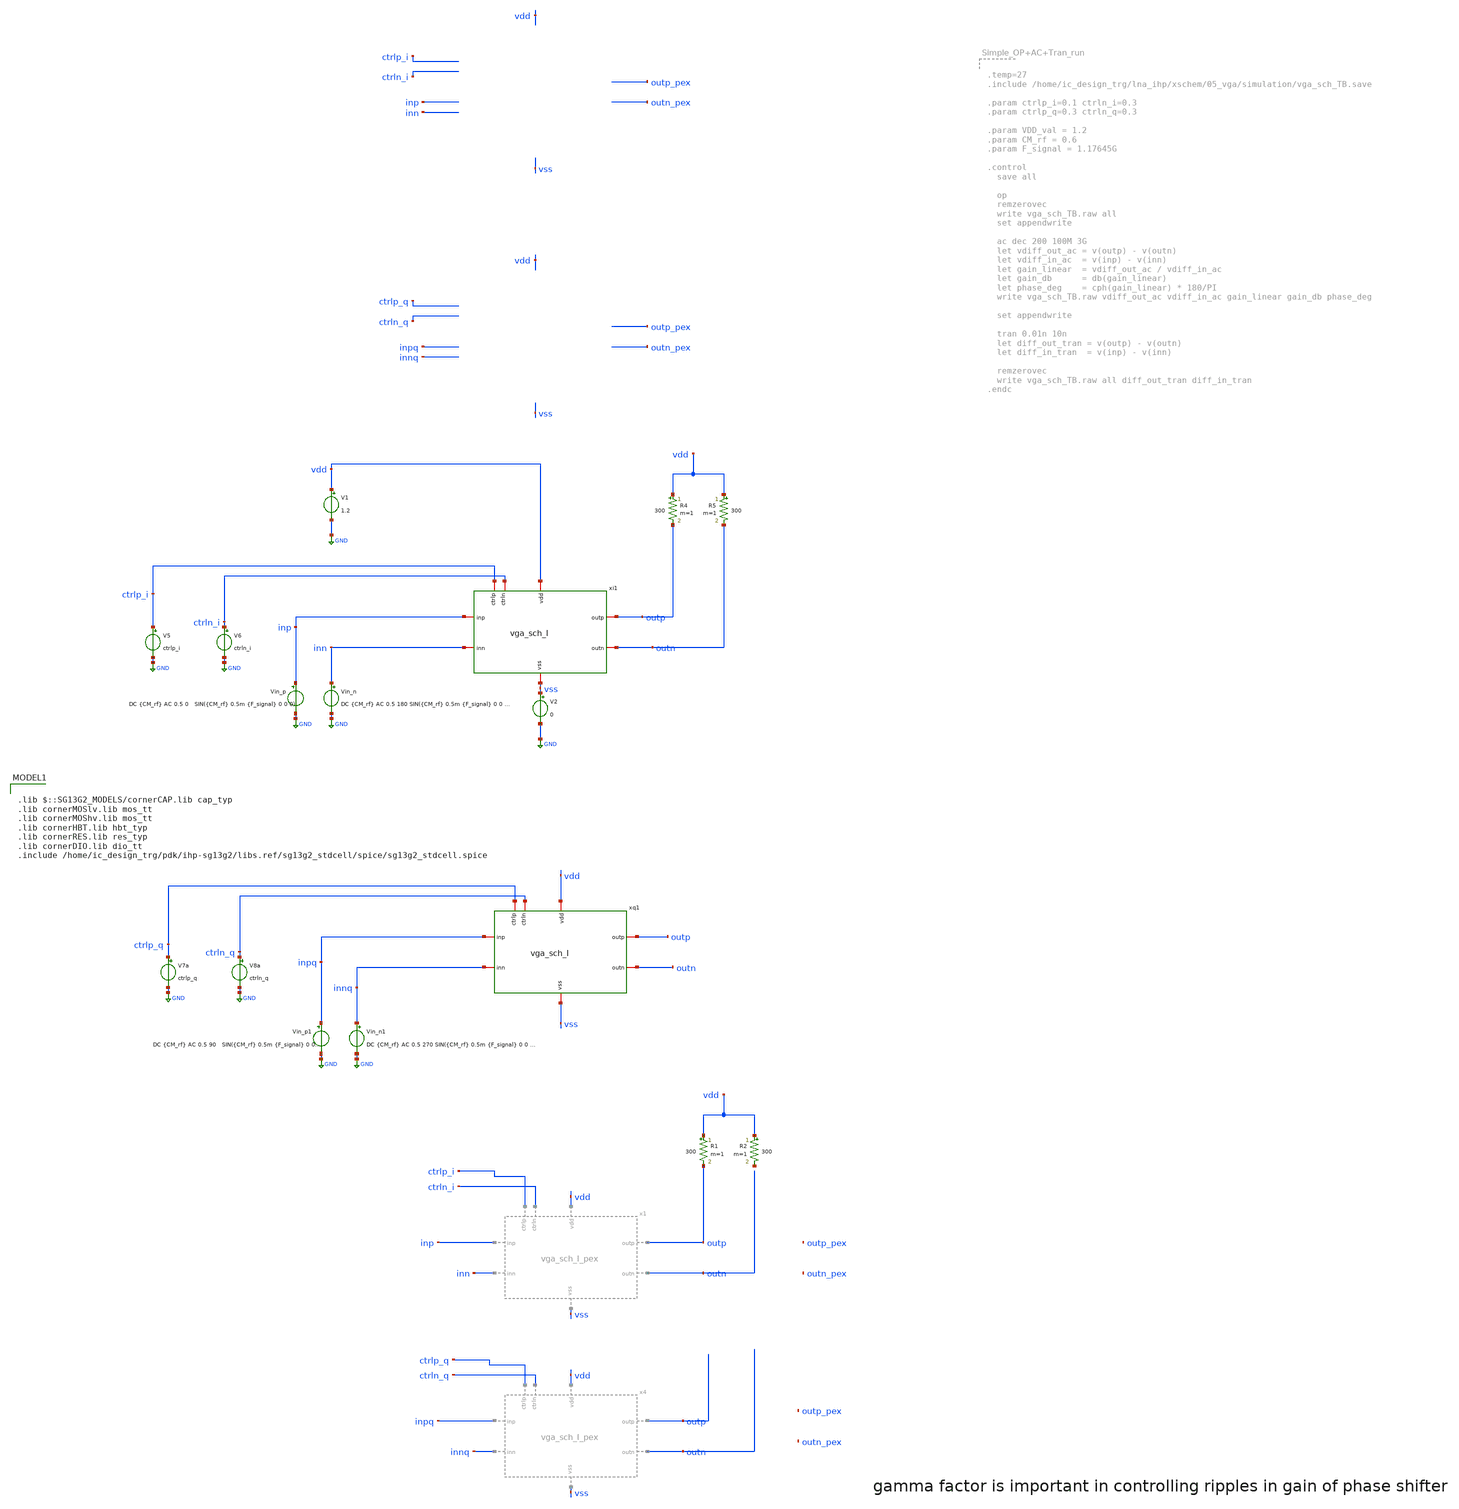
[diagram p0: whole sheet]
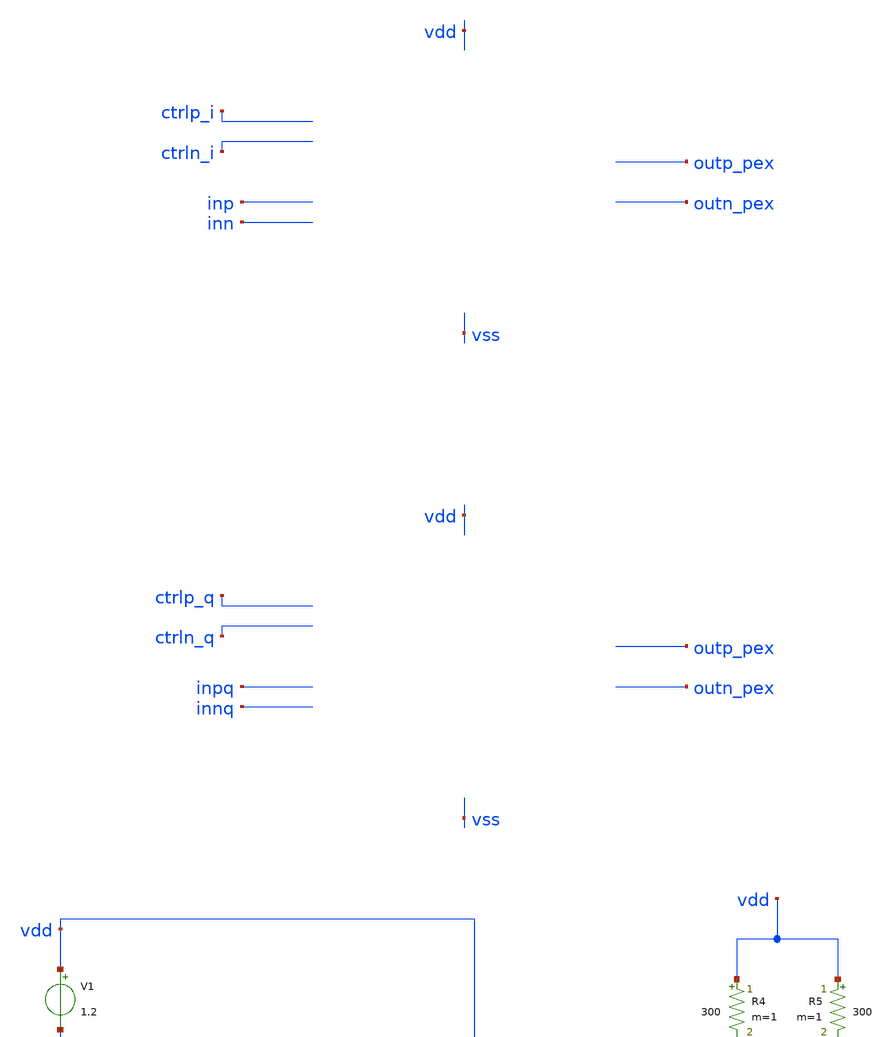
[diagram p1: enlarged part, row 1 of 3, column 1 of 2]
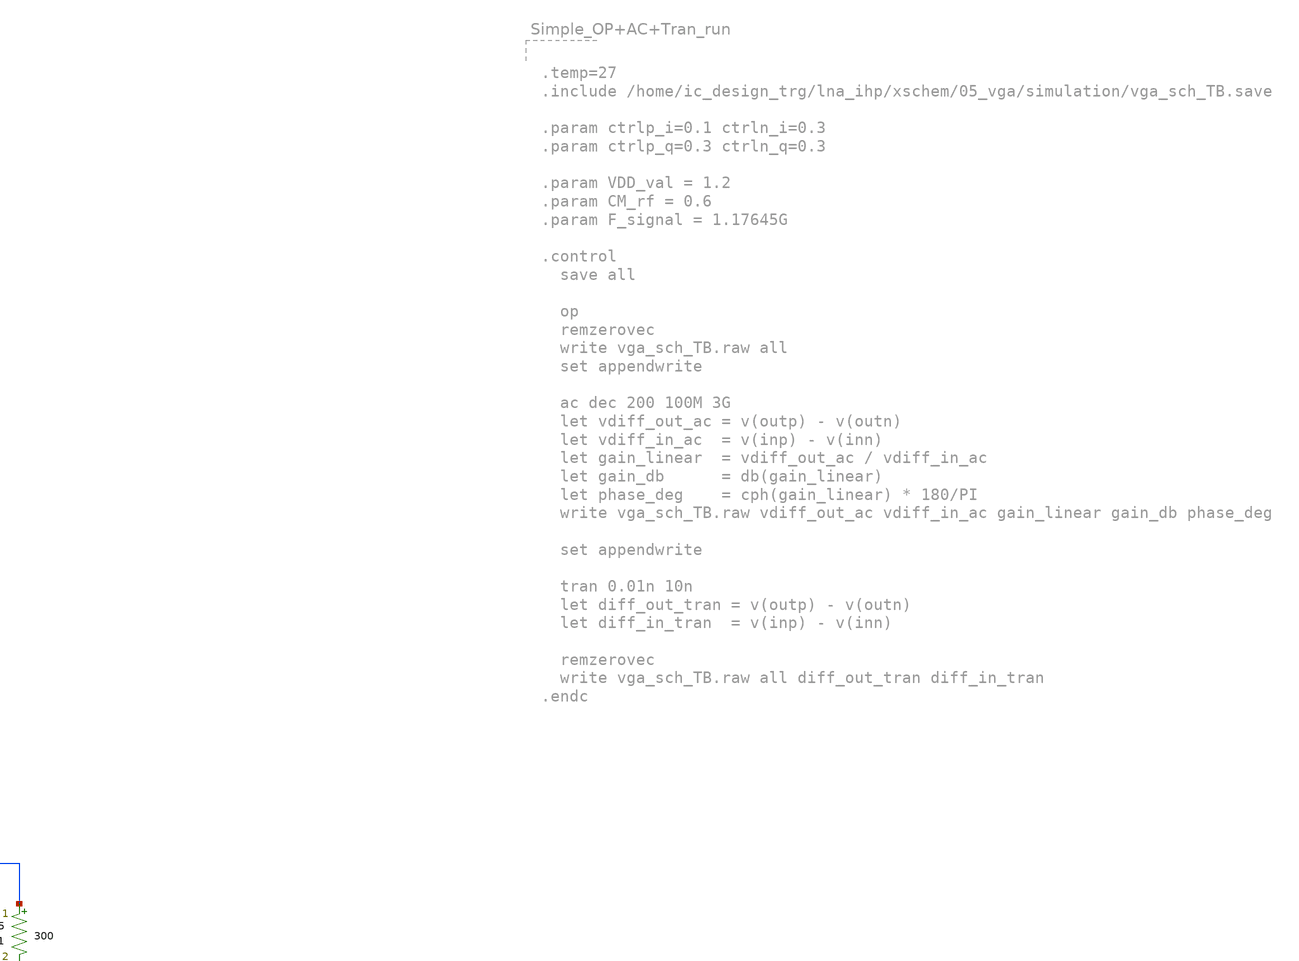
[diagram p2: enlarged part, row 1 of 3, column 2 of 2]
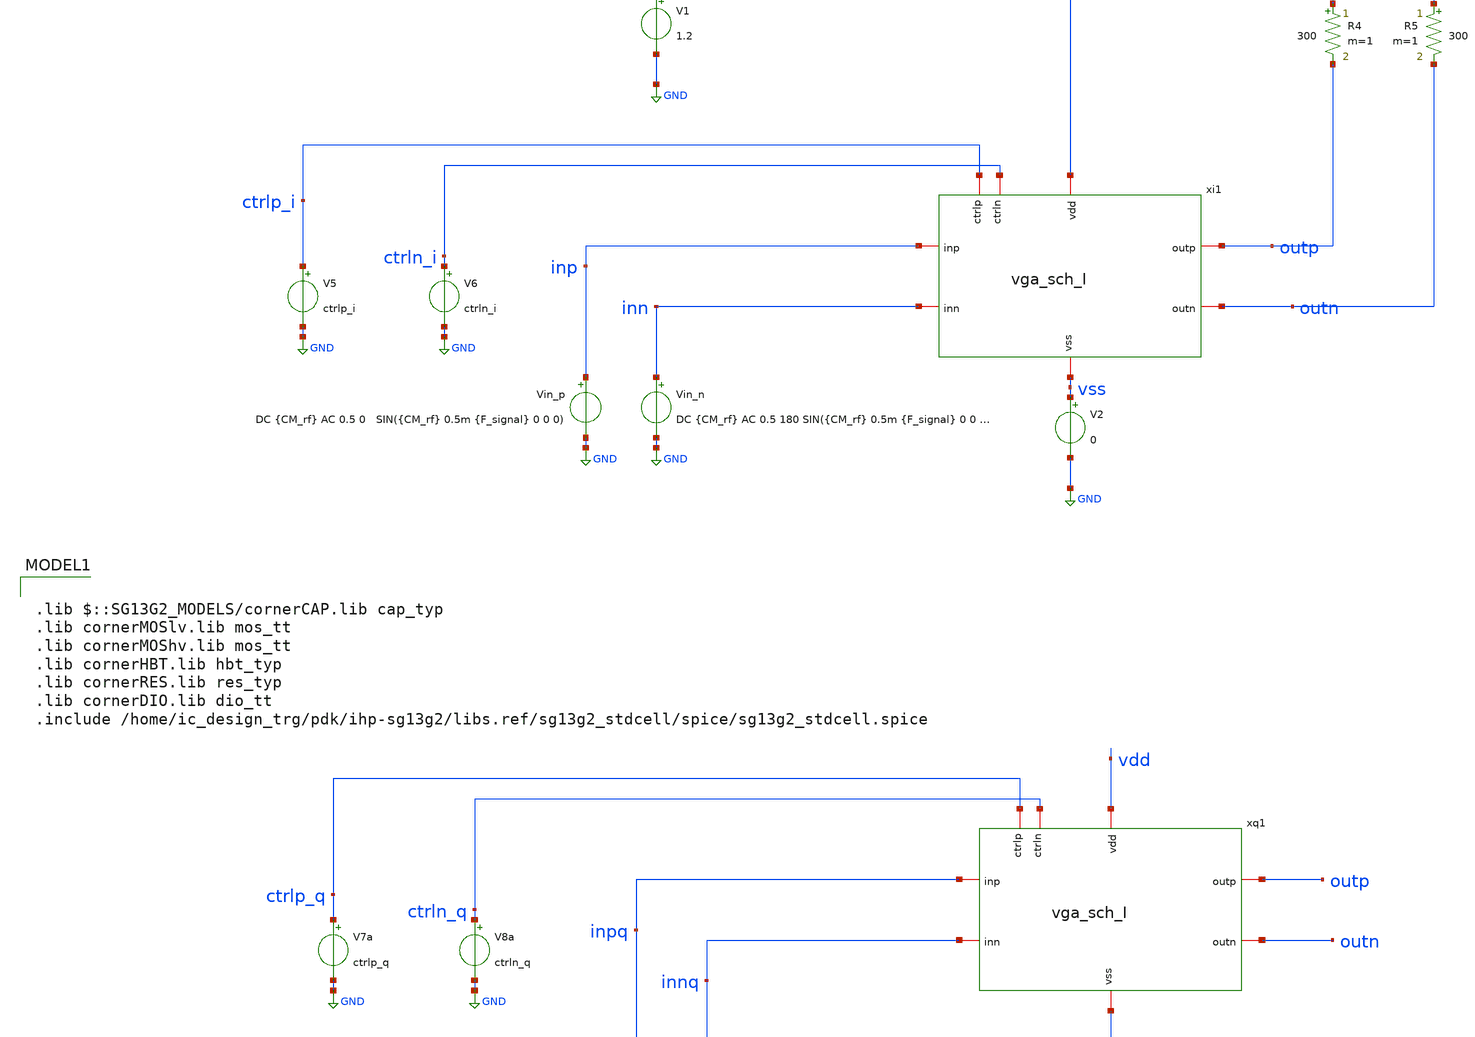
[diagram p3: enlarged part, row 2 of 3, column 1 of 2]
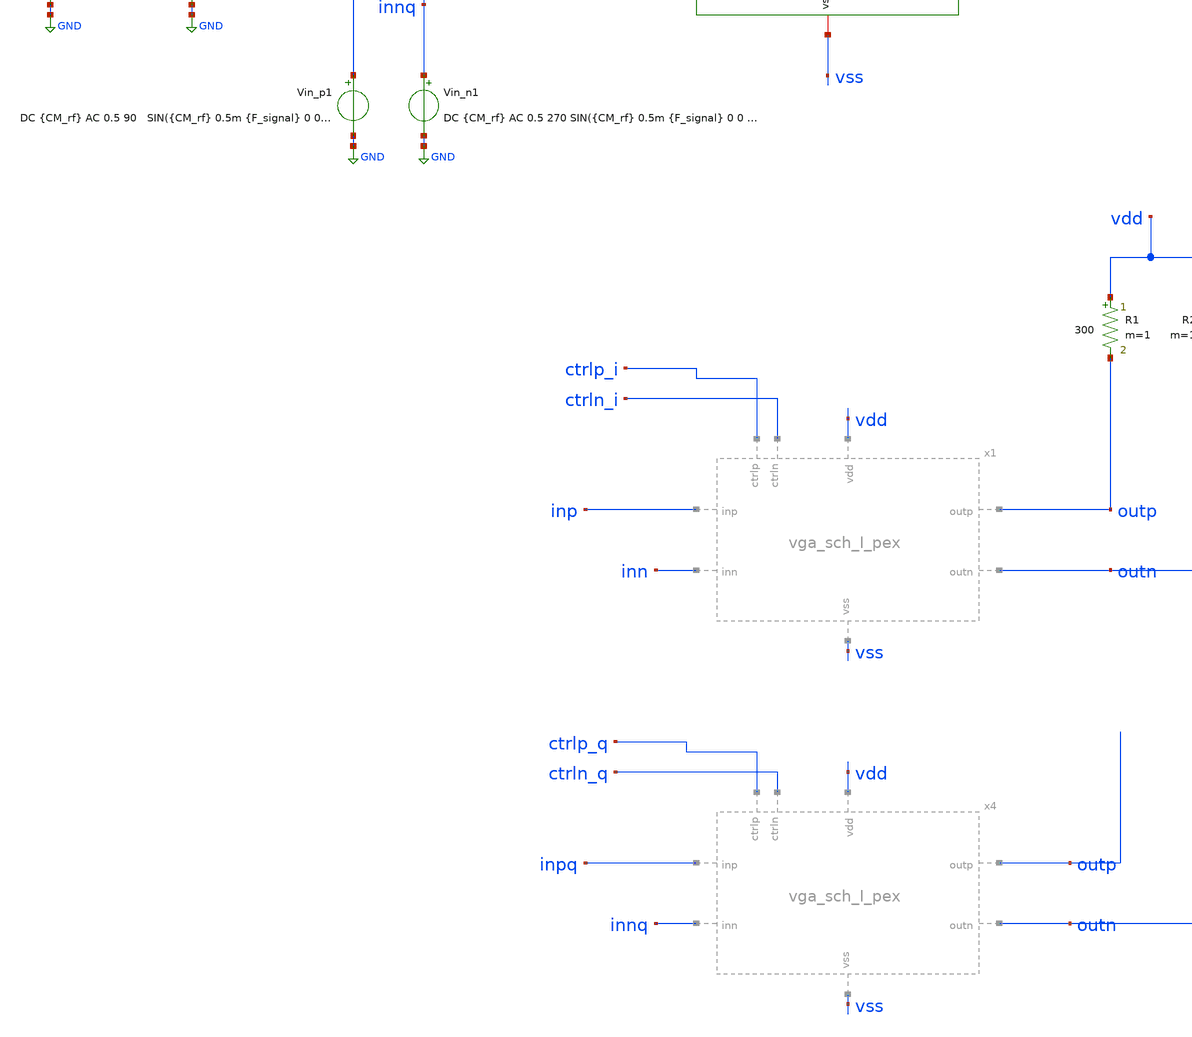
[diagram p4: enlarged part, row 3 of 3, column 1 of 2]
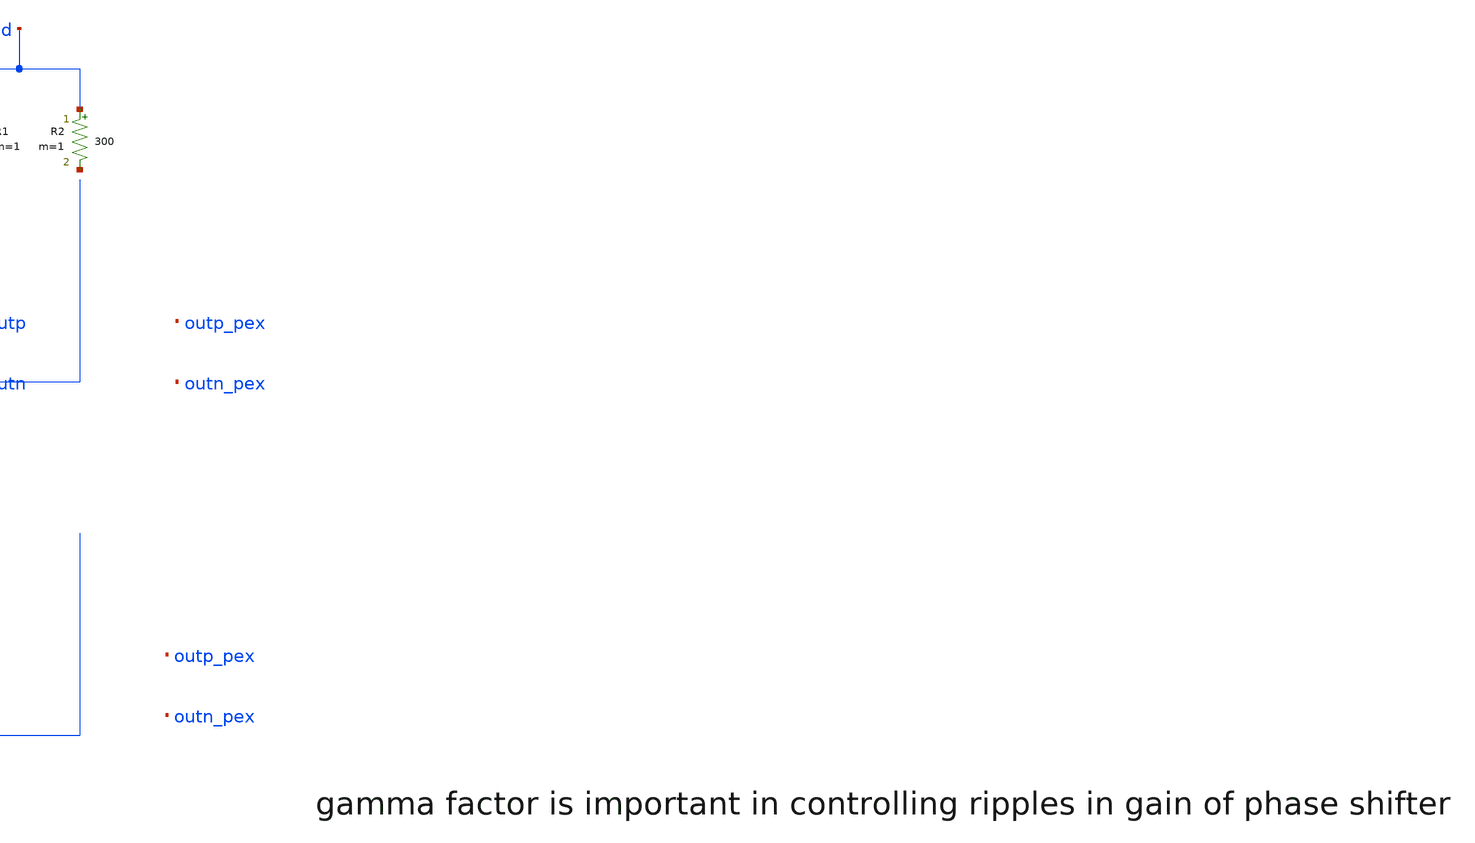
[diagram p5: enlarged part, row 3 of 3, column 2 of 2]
** sch_path: LNA7096-main/schematic/xschem/05_vga/vga_sch_TB.sch
**.subckt vga_sch_TB
Vin_p inp GND DC {CM_rf} AC 0.5 0 SIN({CM_rf} 0.5m {F_signal} 0 0 0)
V1 vdd GND 1.2
V2 vss GND 0
Vin_n inn GND DC {CM_rf} AC 0.5 180 SIN({CM_rf} 0.5m {F_signal} 0 0 180)
V5 ctrlp_i GND ctrlp_i
V6 ctrln_i GND ctrln_i
V7a ctrlp_q GND ctrlp_q
V8a ctrln_q GND ctrln_q
Vin_p1 inpq GND DC {CM_rf} AC 0.5 90 SIN({CM_rf} 0.5m {F_signal} 0 0 90)
Vin_n1 innq GND DC {CM_rf} AC 0.5 270 SIN({CM_rf} 0.5m {F_signal} 0 0 270)
R4 vdd outp 300 m=1
R5 vdd outn 300 m=1
xi1 vdd outp outn ctrln_i ctrlp_i inp inn vss vga_sch_I
xq1 vdd outp outn ctrln_q ctrlp_q inpq innq vss vga_sch_I
R1 vdd outp 300 m=1
R2 vdd net1 300 m=1
**** begin user architecture code

.lib $::SG13G2_MODELS/cornerCAP.lib cap_typ
.lib cornerMOSlv.lib mos_tt
.lib cornerMOShv.lib mos_tt
.lib cornerHBT.lib hbt_typ
.lib cornerRES.lib res_typ
.lib cornerDIO.lib dio_tt
.include /home/ic_design_trg/pdk/ihp-sg13g2/libs.ref/sg13g2_stdcell/spice/sg13g2_stdcell.spice



.temp=27
.include vga_sch_TB.save

.param ctrlp_i=0.3 ctrln_i=0.3
.param ctrlp_q=0.3 ctrln_q=0.3

.param VDD_val = 1.2
.param CM_rf = 0.6
.param F_signal = 1.17645G



.control
  * 1. Setup and Initialization
  save all
  * Ensure we start with a clean state for file writing
  unset appendwrite

  * --- Define Phase Angle and Control Vectors ---
  compose theta_vals start=0 stop=360 step=5.625
  let rad_vec = theta_vals * PI / 180

  * Define Constants
  let v_cm = 0.6
  let v_max = 0.3

  * --- PRE-DISTORTION SETTING ---
  let gamma = 1.35

  * Calculate Raw Weights
  let cos_w = cos(rad_vec)
  let sin_w = sin(rad_vec)

  * --- Corrections for 'sgn' and 'pow' errors ---
  * 1. Use (val gt 0) - (val lt 0) to emulate sgn()
  let sgn_cos = (cos_w gt 0) - (cos_w lt 0)
  let sgn_sin = (sin_w gt 0) - (sin_w lt 0)

  * 2. Use '^' operator instead of pow()
  let i_corr = sgn_cos * (abs(cos_w)^gamma)
  let q_corr = sgn_sin * (abs(sin_w)^gamma)

  * Pre-calculate 4-Quadrant Control Voltages
  let pi_p_vec = v_cm + v_max * i_corr
  let pi_n_vec = v_cm - v_max * i_corr
  let pq_p_vec = v_cm + v_max * q_corr
  let pq_n_vec = v_cm - v_max * q_corr

  * --- Initialize Loop ---
  let n_runs = length(theta_vals)
  let run_idx = 0

  * Capture the start plot (constants) to retrieve vectors later
  set start_plot = $curplot

  * [UPDATED] Create CSV File Header with Control Voltages included
  echo theta,ctrlp_i,ctrln_i,ctrlp_q,ctrln_q,gain_L5,phase_L5 > vmps_corrected_sweep.csv

  * --- Execution Loop ---
  dowhile run_idx < n_runs

    * 1. Retrieve calculated DC voltages from the start plot
    let pip_act = {$start_plot}.pi_p_vec[run_idx]
    let pin_act = {$start_plot}.pi_n_vec[run_idx]
    let pqp_act = {$start_plot}.pq_p_vec[run_idx]
    let pqn_act = {$start_plot}.pq_n_vec[run_idx]
    let t_act = {$start_plot}.theta_vals[run_idx]

    * 2. Apply Bias
    alter V5 dc = $&pip_act
    alter V6 dc = $&pin_act
    alter V7a dc = $&pqp_act
    alter V8a dc = $&pqn_act

    * 3. Run AC Analysis
    ac dec 10 1G 2G

    * 4. Post-Processing & Extraction
    let diff_out = v(outp) - v(outn)
    let gain_lin = mag(diff_out)
    let phase_deg = cph(diff_out) * 180 / PI

    * Measure Gain and Phase at target frequency (1.17645 GHz)
    meas ac m_gain find gain_lin at=1.17645G
    meas ac m_phase find phase_deg at=1.17645G

    * 5. [UPDATED] Write Scalar Results and Control Voltages to CSV
    echo $&t_act,$&pip_act,$&pin_act,$&pqp_act,$&pqn_act,$&m_gain,$&m_phase >>
+ vmps_corrected_sweep.csv

    * 6. Save AC Plots to RAW file for GAW
    * On the first run, create the file. On subsequent runs, append to it.
    if run_idx = 0
       write vga_sch_TB.raw all
       set appendwrite
    else
       write vga_sch_TB.raw all
    end

    * Cleanup: Destroy the current AC plot to free RAM.
    destroy $curplot

    let run_idx = run_idx + 1
  end


.endc



**** end user architecture code
**.ends

* expanding   symbol:  05_vga/vga_sch_I_pex.sym # of pins=8
** sym_path: LNA7096-main/schematic/xschem/05_vga/vga_sch_I.sym
.include /home/ic_design_trg/lna_ihp/klayout/05_vga/output/vga_sch_I_flat__vga_sch_I/magic_RC/vga_sch_I.pex.spice

* expanding   symbol:  05_vga/vga_sch_I.sym # of pins=8
** sym_path: LNA7096-main/schematic/xschem/05_vga/vga_sch_I.sym
** sch_path: LNA7096-main/schematic/xschem/05_vga/vga_sch_I.sch
.subckt vga_sch_I vdd outp outn ctrln ctrlp inp inn vss
*.iopin vdd
*.iopin vss
*.iopin inp
*.iopin outp
*.iopin outn
*.iopin ctrlp
*.iopin ctrln
*.iopin inn
XR7 vdd a4 vss rhigh w=1e-6 l=15.71e-6 m=1 b=0 mm_ok=1
XR1 a3 vss vss rhigh w=1e-6 l=13.5e-6 m=1 b=0 mm_ok=1
XR2 vdd a3 vss rhigh w=1e-6 l=15.71e-6 m=1 b=0 mm_ok=1
XR10 vdd a2 vss rhigh w=1e-6 l=14.21e-6 m=1 b=0 mm_ok=1
XR12 a1 vss vss rhigh w=1e-6 l=44.8e-6 m=1 b=0 mm_ok=1
XR13 a1 vdd vss rhigh w=1e-6 l=14.21e-6 m=1 b=0 mm_ok=1
XC4 inp inp_b cap_cmim w=46.85e-6 l=46.85e-6 m=4 mm_ok=1
XR14 a1 inp_b vss rhigh w=1e-6 l=35.1e-6 m=1 b=0 mm_ok=1
XR18 bias_p vss vss rhigh w=1e-6 l=1.05e-6 m=1 b=0 mm_ok=1
XC2 inn inn_b cap_cmim w=46.85e-6 l=46.85e-6 m=4 mm_ok=1
XC11 inp inp_a cap_cmim w=46.85e-6 l=46.85e-6 m=4 mm_ok=1
XC1 inn inn_a cap_cmim w=46.85e-6 l=46.85e-6 m=4 mm_ok=1
XM2 bias_p bias_p vdd vdd sg13_lv_pmos w=49.98u l=0.3u ng=20 m=1 mm_ok=1
XM1 n3 bias_p vdd vdd sg13_lv_pmos w=700u l=0.3u ng=100 m=1 mm_ok=1
XM3 n1 ctrlp n3 n3 sg13_lv_pmos w=150u l=0.3u ng=20 m=1 mm_ok=1
XM4 n2 ctrln n3 n3 sg13_lv_pmos w=150u l=0.3u ng=20 m=1 mm_ok=1
XM5 outp inp_b n1 net1 sg13_lv_nmos w=120u l=0.25u ng=20 m=1 mm_ok=1
XM6 outn inn_b n1 net2 sg13_lv_nmos w=120u l=0.25u ng=20 m=1 mm_ok=1
XM7 outn inp_b n2 net4 sg13_lv_nmos w=120u l=0.25u ng=20 m=1 mm_ok=1
XM8 outp inn_b n2 net3 sg13_lv_nmos w=120u l=0.25u ng=20 m=1 mm_ok=1
XM9 n1 inp_a vss vss sg13_lv_nmos w=40u l=0.25u ng=10 m=1 mm_ok=1
XM10 n1 inn_a vss vss sg13_lv_nmos w=40u l=0.25u ng=10 m=1 mm_ok=1
XM11 n2 inn_a vss vss sg13_lv_nmos w=40u l=0.25u ng=10 m=1 mm_ok=1
XM12 n2 inp_a vss vss sg13_lv_nmos w=40u l=0.25u ng=10 m=1 mm_ok=1
XD4 net2 vdd vss isolbox l=24.12u w=10u
XD5 net1 vdd vss isolbox l=24.12u w=10u
XR22 n1 net1 ptap1 R=94.78 w=0.39e-6 l=4e-6
XR15 n1 net2 ptap1 R=94.78 w=0.39e-6 l=4e-6
XD3 net4 vdd vss isolbox l=24.12u w=10u
XD6 net3 vdd vss isolbox l=24.12u w=10u
XR16 n2 net3 ptap1 R=94.78 w=0.39e-6 l=4e-6
XR23 n2 net4 ptap1 R=94.78 w=0.39e-6 l=4e-6
XR4 a2 vss vss rhigh w=1e-6 l=44.8e-6 m=1 b=0 mm_ok=1
XR5 a2 inn_b vss rhigh w=1e-6 l=35.1e-6 m=1 b=0 mm_ok=1
XR6 a4 vss vss rhigh w=1e-6 l=13.5e-6 m=1 b=0 mm_ok=1
XR3 a3 inp_a vss rhigh w=1e-6 l=35.1e-6 m=1 b=0 mm_ok=1
XR8 a4 inn_a vss rhigh w=1e-6 l=35.1e-6 m=1 b=0 mm_ok=1
.ends

.GLOBAL GND
.end
